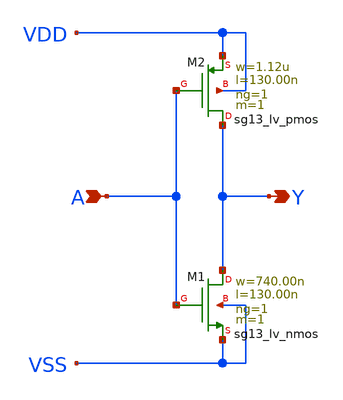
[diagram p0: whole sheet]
** sch_path: ihp-sg13g2/libs.ref/sg13g2_stdcell/sch/xschem/sg13g2_inv_1.sch
* Copyright 2023 IHP PDK Authors
* Licensed under the Apache License, Version 2.0 (the "License");
* you may not use this file except in compliance with the License.
* You may obtain a copy of the License at
* https://www.apache.org/licenses/LICENSE-2.0
* Unless required by applicable law or agreed to in writing, software
* distributed under the License is distributed on an "AS IS" BASIS,
* WITHOUT WARRANTIES OR CONDITIONS OF ANY KIND, either express or implied.
* See the License for the specific language governing permissions and
* limitations under the License.
**.subckt sg13g2_inv_1 Y A
*.opin Y
*.ipin A
XM1 Y A VSS VSS sg13_lv_nmos w=740.00n l=130.00n ng=1 m=1 mm_ok=1
XM2 Y A VDD VDD sg13_lv_pmos w=1.12u l=130.00n ng=1 m=1 mm_ok=1
**.ends
.end
